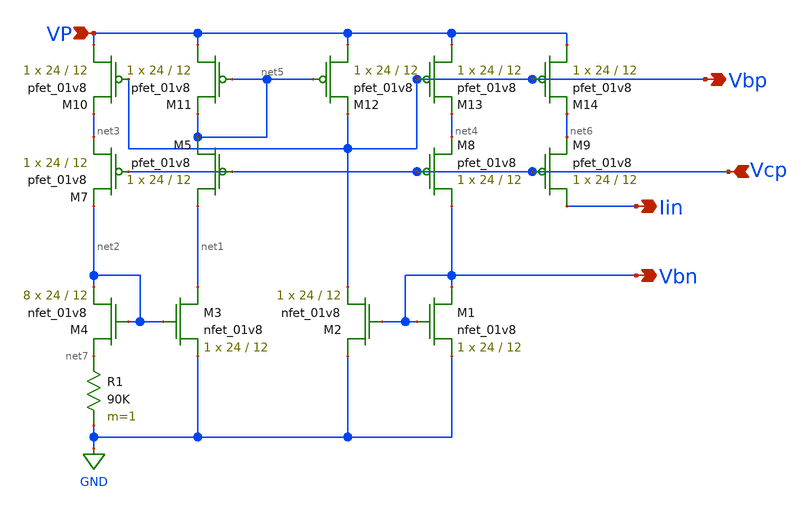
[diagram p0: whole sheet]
** sch_path: xschem/a_new_curgen-1.sch
**.subckt a_new_curgen-1 Iin VP Vbp Vbn Vcp
*.opin Iin
*.ipin VP
*.opin Vbp
*.opin Vbn
*.ipin Vcp
XM1 Vbn Vbn GND GND sky130_fd_pr__nfet_01v8 L=12 W=24 nf=1 ad='int((nf+1)/2) * W/nf * 0.29' as='int((nf+2)/2) * W/nf * 0.29'
+ pd='2*int((nf+1)/2) * (W/nf + 0.29)' ps='2*int((nf+2)/2) * (W/nf + 0.29)' nrd='0.29 / W' nrs='0.29 / W'
+ sa=0 sb=0 sd=0 mult=1 m=1
XM2 GND Vbn Vbp GND sky130_fd_pr__nfet_01v8 L=12 W=24 nf=1 ad='int((nf+1)/2) * W/nf * 0.29' as='int((nf+2)/2) * W/nf * 0.29'
+ pd='2*int((nf+1)/2) * (W/nf + 0.29)' ps='2*int((nf+2)/2) * (W/nf + 0.29)' nrd='0.29 / W' nrs='0.29 / W'
+ sa=0 sb=0 sd=0 mult=1 m=1
XM3 net1 net2 GND GND sky130_fd_pr__nfet_01v8 L=12 W=24 nf=1 ad='int((nf+1)/2) * W/nf * 0.29' as='int((nf+2)/2) * W/nf * 0.29'
+ pd='2*int((nf+1)/2) * (W/nf + 0.29)' ps='2*int((nf+2)/2) * (W/nf + 0.29)' nrd='0.29 / W' nrs='0.29 / W'
+ sa=0 sb=0 sd=0 mult=1 m=1
XM4 net7 net2 net2 GND sky130_fd_pr__nfet_01v8 L=12 W=24 nf=1 ad='int((nf+1)/2) * W/nf * 0.29' as='int((nf+2)/2) * W/nf * 0.29'
+ pd='2*int((nf+1)/2) * (W/nf + 0.29)' ps='2*int((nf+2)/2) * (W/nf + 0.29)' nrd='0.29 / W' nrs='0.29 / W'
+ sa=0 sb=0 sd=0 mult=8 m=8
XM7 net3 Vcp net2 VDD sky130_fd_pr__pfet_01v8 L=12 W=24 nf=1 ad='int((nf+1)/2) * W/nf * 0.29' as='int((nf+2)/2) * W/nf * 0.29'
+ pd='2*int((nf+1)/2) * (W/nf + 0.29)' ps='2*int((nf+2)/2) * (W/nf + 0.29)' nrd='0.29 / W' nrs='0.29 / W'
+ sa=0 sb=0 sd=0 mult=1 m=1
XM8 Vbn Vcp net4 VDD sky130_fd_pr__pfet_01v8 L=12 W=24 nf=1 ad='int((nf+1)/2) * W/nf * 0.29' as='int((nf+2)/2) * W/nf * 0.29'
+ pd='2*int((nf+1)/2) * (W/nf + 0.29)' ps='2*int((nf+2)/2) * (W/nf + 0.29)' nrd='0.29 / W' nrs='0.29 / W'
+ sa=0 sb=0 sd=0 mult=1 m=1
R1 net7 GND 90K m=1
XM9 Iin Vcp net6 VDD sky130_fd_pr__pfet_01v8 L=12 W=24 nf=1 ad='int((nf+1)/2) * W/nf * 0.29' as='int((nf+2)/2) * W/nf * 0.29'
+ pd='2*int((nf+1)/2) * (W/nf + 0.29)' ps='2*int((nf+2)/2) * (W/nf + 0.29)' nrd='0.29 / W' nrs='0.29 / W'
+ sa=0 sb=0 sd=0 mult=1 m=1
XM10 VP Vbp net3 VDD sky130_fd_pr__pfet_01v8 L=12 W=24 nf=1 ad='int((nf+1)/2) * W/nf * 0.29' as='int((nf+2)/2) * W/nf * 0.29'
+ pd='2*int((nf+1)/2) * (W/nf + 0.29)' ps='2*int((nf+2)/2) * (W/nf + 0.29)' nrd='0.29 / W' nrs='0.29 / W'
+ sa=0 sb=0 sd=0 mult=1 m=1
XM11 VP net5 net5 VDD sky130_fd_pr__pfet_01v8 L=12 W=24 nf=1 ad='int((nf+1)/2) * W/nf * 0.29' as='int((nf+2)/2) * W/nf * 0.29'
+ pd='2*int((nf+1)/2) * (W/nf + 0.29)' ps='2*int((nf+2)/2) * (W/nf + 0.29)' nrd='0.29 / W' nrs='0.29 / W'
+ sa=0 sb=0 sd=0 mult=1 m=1
XM12 VP net5 Vbp VDD sky130_fd_pr__pfet_01v8 L=12 W=24 nf=1 ad='int((nf+1)/2) * W/nf * 0.29' as='int((nf+2)/2) * W/nf * 0.29'
+ pd='2*int((nf+1)/2) * (W/nf + 0.29)' ps='2*int((nf+2)/2) * (W/nf + 0.29)' nrd='0.29 / W' nrs='0.29 / W'
+ sa=0 sb=0 sd=0 mult=1 m=1
XM13 VP Vbp net4 VDD sky130_fd_pr__pfet_01v8 L=12 W=24 nf=1 ad='int((nf+1)/2) * W/nf * 0.29' as='int((nf+2)/2) * W/nf * 0.29'
+ pd='2*int((nf+1)/2) * (W/nf + 0.29)' ps='2*int((nf+2)/2) * (W/nf + 0.29)' nrd='0.29 / W' nrs='0.29 / W'
+ sa=0 sb=0 sd=0 mult=1 m=1
XM14 VP Vbp net6 VDD sky130_fd_pr__pfet_01v8 L=12 W=24 nf=1 ad='int((nf+1)/2) * W/nf * 0.29' as='int((nf+2)/2) * W/nf * 0.29'
+ pd='2*int((nf+1)/2) * (W/nf + 0.29)' ps='2*int((nf+2)/2) * (W/nf + 0.29)' nrd='0.29 / W' nrs='0.29 / W'
+ sa=0 sb=0 sd=0 mult=1 m=1
XM5 net1 Vcp net5 VDD sky130_fd_pr__pfet_01v8 L=12 W=24 nf=1 ad='int((nf+1)/2) * W/nf * 0.29' as='int((nf+2)/2) * W/nf * 0.29'
+ pd='2*int((nf+1)/2) * (W/nf + 0.29)' ps='2*int((nf+2)/2) * (W/nf + 0.29)' nrd='0.29 / W' nrs='0.29 / W'
+ sa=0 sb=0 sd=0 mult=1 m=1
**.ends
.GLOBAL GND
.end
